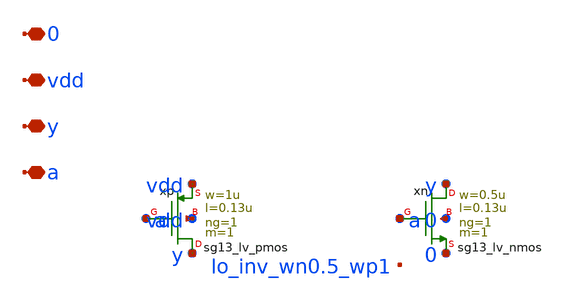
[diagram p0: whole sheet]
** sch_path: analog/lo/sch/lo_inv_05_1.sch
**.subckt lo_inv_05_1 a y vdd 0
*.iopin a
*.iopin y
*.iopin vdd
*.iopin 0
Xxp y a vdd vdd sg13_lv_pmos w=1u l=0.13u ng=1 m=1 mm_ok=1
Xxn y a 0 0 sg13_lv_nmos w=0.5u l=0.13u ng=1 m=1 mm_ok=1
**.ends
.end
